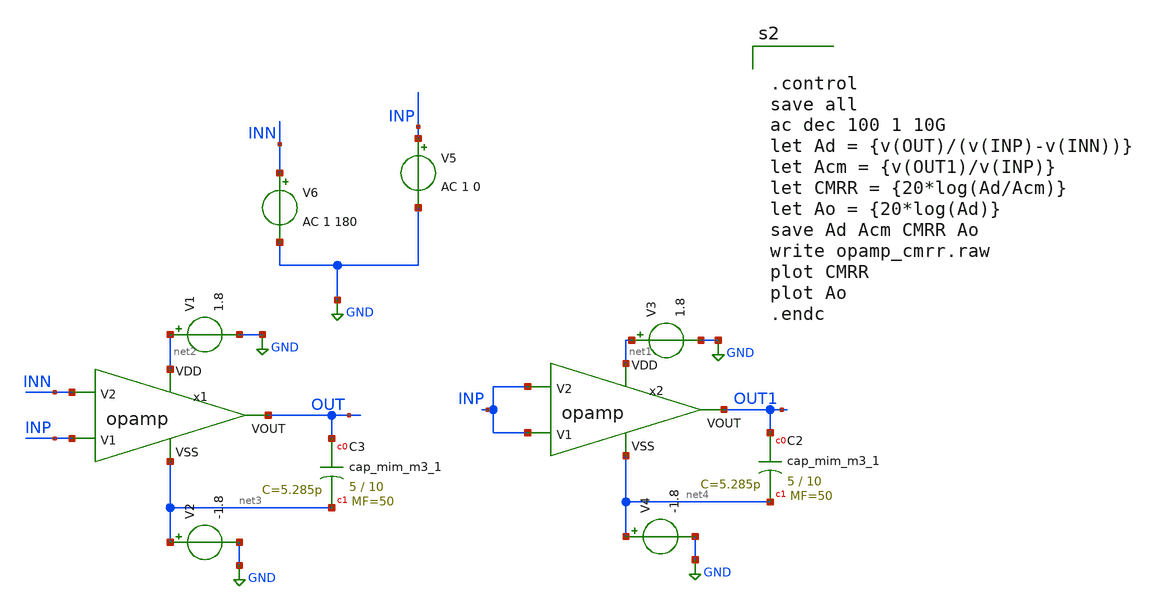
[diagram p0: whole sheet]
** sch_path: xschem/opamp_cmrr_ff.sch
**.subckt opamp_cmrr_ff
V6 INN GND AC 1 180
V5 INP GND AC 1 0
V1 net2 GND 1.8
V2 net3 GND -1.8
V3 net1 GND 1.8
V4 net4 GND -1.8
XC2 OUT1 net4 sky130_fd_pr__cap_mim_m3_1 W=5 L=10 MF=50 m=50
XC3 OUT net3 sky130_fd_pr__cap_mim_m3_1 W=5 L=10 MF=50 m=50
x1 net2 net3 INP INN OUT opamp
x2 net1 net4 INP INP OUT1 opamp
**** begin user architecture code


.control
save all
ac dec 100 1 10G
let Ad = {v(OUT)/(v(INP)-v(INN))}
let Acm = {v(OUT1)/v(INP)}
let CMRR = {20*log(Ad/Acm)}
let Ao = {20*log(Ad)}
save Ad Acm CMRR Ao
write opamp_cmrr.raw
plot CMRR
plot Ao
.endc



** opencircuitdesign pdks install
.lib $::SKYWATER_MODELS/sky130.lib.spice ff


**** end user architecture code
**.ends

* expanding   symbol:  /foss/designs/chipalooza2024/sky130_hcmus_ip__instramp/xschem/opamp.sym # of
*+ pins=5
** sym_path: /foss/designs/chipalooza2024/sky130_hcmus_ip__instramp/xschem/opamp.sym
** sch_path: /foss/designs/chipalooza2024/sky130_hcmus_ip__instramp/xschem/opamp.sch
.subckt opamp VDD VSS V1 V2 VOUT
*.ipin VSS
*.ipin VDD
*.ipin V2
*.ipin V1
*.opin VOUT
XM2 net5 V2 net1 VSS sky130_fd_pr__nfet_g5v0d10v5 L=1 W=18 nf=1 ad='int((nf+1)/2) * W/nf * 0.29' as='int((nf+2)/2) * W/nf * 0.29'
+ pd='2*int((nf+1)/2) * (W/nf + 0.29)' ps='2*int((nf+2)/2) * (W/nf + 0.29)' nrd='0.29 / W' nrs='0.29 / W'
+ sa=0 sb=0 sd=0 mult=1 m=1
XM1 net6 net5 VDD VDD sky130_fd_pr__pfet_g5v0d10v5 L=1 W=30 nf=1 ad='int((nf+1)/2) * W/nf * 0.29' as='int((nf+2)/2) * W/nf * 0.29'
+ pd='2*int((nf+1)/2) * (W/nf + 0.29)' ps='2*int((nf+2)/2) * (W/nf + 0.29)' nrd='0.29 / W' nrs='0.29 / W'
+ sa=0 sb=0 sd=0 mult=1 m=1
XM4 net6 V1 net1 VSS sky130_fd_pr__nfet_g5v0d10v5 L=1 W=18 nf=1 ad='int((nf+1)/2) * W/nf * 0.29' as='int((nf+2)/2) * W/nf * 0.29'
+ pd='2*int((nf+1)/2) * (W/nf + 0.29)' ps='2*int((nf+2)/2) * (W/nf + 0.29)' nrd='0.29 / W' nrs='0.29 / W'
+ sa=0 sb=0 sd=0 mult=1 m=1
XM5 net1 net4 VSS VSS sky130_fd_pr__nfet_g5v0d10v5 L=1 W=15.171 nf=1 ad='int((nf+1)/2) * W/nf * 0.29'
+ as='int((nf+2)/2) * W/nf * 0.29' pd='2*int((nf+1)/2) * (W/nf + 0.29)' ps='2*int((nf+2)/2) * (W/nf + 0.29)'
+ nrd='0.29 / W' nrs='0.29 / W' sa=0 sb=0 sd=0 mult=1 m=1
XM6 VOUT net4 VSS VSS sky130_fd_pr__nfet_g5v0d10v5 L=1 W=19 nf=1 ad='int((nf+1)/2) * W/nf * 0.29' as='int((nf+2)/2) * W/nf * 0.29'
+ pd='2*int((nf+1)/2) * (W/nf + 0.29)' ps='2*int((nf+2)/2) * (W/nf + 0.29)' nrd='0.29 / W' nrs='0.29 / W'
+ sa=0 sb=0 sd=0 mult=1 m=1
XM7 net4 net4 VSS VSS sky130_fd_pr__nfet_g5v0d10v5 L=1 W=20 nf=1 ad='int((nf+1)/2) * W/nf * 0.29' as='int((nf+2)/2) * W/nf * 0.29'
+ pd='2*int((nf+1)/2) * (W/nf + 0.29)' ps='2*int((nf+2)/2) * (W/nf + 0.29)' nrd='0.29 / W' nrs='0.29 / W'
+ sa=0 sb=0 sd=0 mult=1 m=1
XM3 net5 net5 VDD VDD sky130_fd_pr__pfet_g5v0d10v5 L=1 W=30 nf=1 ad='int((nf+1)/2) * W/nf * 0.29' as='int((nf+2)/2) * W/nf * 0.29'
+ pd='2*int((nf+1)/2) * (W/nf + 0.29)' ps='2*int((nf+2)/2) * (W/nf + 0.29)' nrd='0.29 / W' nrs='0.29 / W'
+ sa=0 sb=0 sd=0 mult=1 m=1
XM8 VOUT net6 VDD VDD sky130_fd_pr__pfet_g5v0d10v5 L=1 W=38 nf=1 ad='int((nf+1)/2) * W/nf * 0.29' as='int((nf+2)/2) * W/nf * 0.29'
+ pd='2*int((nf+1)/2) * (W/nf + 0.29)' ps='2*int((nf+2)/2) * (W/nf + 0.29)' nrd='0.29 / W' nrs='0.29 / W'
+ sa=0 sb=0 sd=0 mult=2 m=2
XR3 net2 VDD VSS sky130_fd_pr__res_high_po W=1 L=30 mult=1 m=1
XR1 net3 net2 VSS sky130_fd_pr__res_high_po W=1 L=30 mult=1 m=1
XR2 net4 net3 VSS sky130_fd_pr__res_high_po W=1 L=30 mult=1 m=1
XR4 net7 VOUT VSS sky130_fd_pr__res_high_po W=1 L=5 mult=1 m=1
XC1 net7 net6 sky130_fd_pr__cap_mim_m3_1 W=5.5 L=10 MF=10 m=10
.ends

.GLOBAL GND
.end
